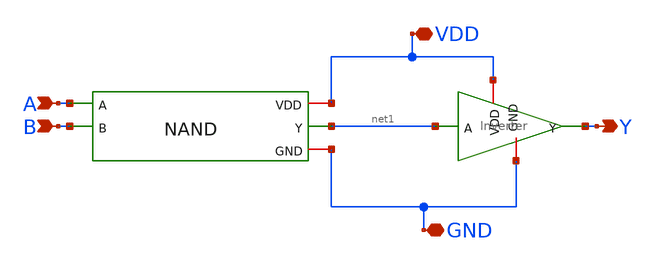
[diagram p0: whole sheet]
** sch_path: AND/AND.sch
**.subckt AND A B VDD Y GND
*.ipin A
*.ipin B
*.iopin VDD
*.opin Y
*.iopin GND
x1 VDD A net1 B GND NAND
x2 VDD net1 Y GND Inverter
**.ends

* expanding   symbol:  /home/ee431/workspace/NAND/NAND.sym # of pins=5
** sym_path: NAND/NAND.sym
** sch_path: NAND/NAND.sch
.subckt NAND VDD A Y B GND
*.ipin A
*.opin Y
*.iopin VDD
*.iopin GND
*.ipin B
XM4 Y A VDD VDD sky130_fd_pr__pfet_01v8 L=0.5 W=2 nf=1 ad='int((nf+1)/2) * W/nf * 0.29' as='int((nf+2)/2) * W/nf * 0.29'
+ pd='2*int((nf+1)/2) * (W/nf + 0.29)' ps='2*int((nf+2)/2) * (W/nf + 0.29)' nrd='0.29 / W' nrs='0.29 / W'
+ sa=0 sb=0 sd=0 mult=1 m=1
XM3 Y B VDD VDD sky130_fd_pr__pfet_01v8 L=0.5 W=2 nf=1 ad='int((nf+1)/2) * W/nf * 0.29' as='int((nf+2)/2) * W/nf * 0.29'
+ pd='2*int((nf+1)/2) * (W/nf + 0.29)' ps='2*int((nf+2)/2) * (W/nf + 0.29)' nrd='0.29 / W' nrs='0.29 / W'
+ sa=0 sb=0 sd=0 mult=1 m=1
XM2 Y B net1 GND sky130_fd_pr__nfet_01v8 L=0.5 W=2 nf=1 ad='int((nf+1)/2) * W/nf * 0.29' as='int((nf+2)/2) * W/nf * 0.29'
+ pd='2*int((nf+1)/2) * (W/nf + 0.29)' ps='2*int((nf+2)/2) * (W/nf + 0.29)' nrd='0.29 / W' nrs='0.29 / W'
+ sa=0 sb=0 sd=0 mult=1 m=1
XM1 net1 A GND GND sky130_fd_pr__nfet_01v8 L=0.5 W=2 nf=1 ad='int((nf+1)/2) * W/nf * 0.29' as='int((nf+2)/2) * W/nf * 0.29'
+ pd='2*int((nf+1)/2) * (W/nf + 0.29)' ps='2*int((nf+2)/2) * (W/nf + 0.29)' nrd='0.29 / W' nrs='0.29 / W'
+ sa=0 sb=0 sd=0 mult=1 m=1
.ends


* expanding   symbol:  /home/ee431/workspace/inverter/Inverter.sym # of pins=4
** sym_path: inverter/Inverter.sym
** sch_path: inverter/Inverter.sch
.subckt Inverter VDD A Y GND
*.ipin A
*.opin Y
*.iopin VDD
*.iopin GND
XM1 Y A VDD VDD sky130_fd_pr__pfet_01v8 L=0.5 W=2 nf=1 ad='int((nf+1)/2) * W/nf * 0.29' as='int((nf+2)/2) * W/nf * 0.29'
+ pd='2*int((nf+1)/2) * (W/nf + 0.29)' ps='2*int((nf+2)/2) * (W/nf + 0.29)' nrd='0.29 / W' nrs='0.29 / W'
+ sa=0 sb=0 sd=0 mult=1 m=1
XM2 Y A GND GND sky130_fd_pr__nfet_01v8 L=0.5 W=1 nf=1 ad='int((nf+1)/2) * W/nf * 0.29' as='int((nf+2)/2) * W/nf * 0.29'
+ pd='2*int((nf+1)/2) * (W/nf + 0.29)' ps='2*int((nf+2)/2) * (W/nf + 0.29)' nrd='0.29 / W' nrs='0.29 / W'
+ sa=0 sb=0 sd=0 mult=1 m=1
.ends

.end
